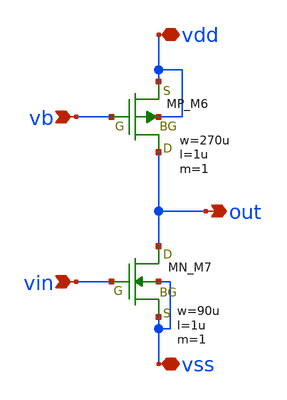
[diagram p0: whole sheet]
** sch_path: OpenSUSI-TR10/opamp/cs.sch
**.subckt cs vb vin out vss vdd
*.ipin vb
*.ipin vin
*.opin out
*.iopin vss
*.iopin vdd
XM6 out vb vdd vdd PMOS w=270u l=1u as=0 ad=0 ps=0 pd=0 nrd=0 nrs=0 m=1
XM7 out vin vss vss NMOS w=90u l=1u as=0 ad=0 ps=0 pd=0 nrd=0 nrs=0 m=1
**.ends
.end
